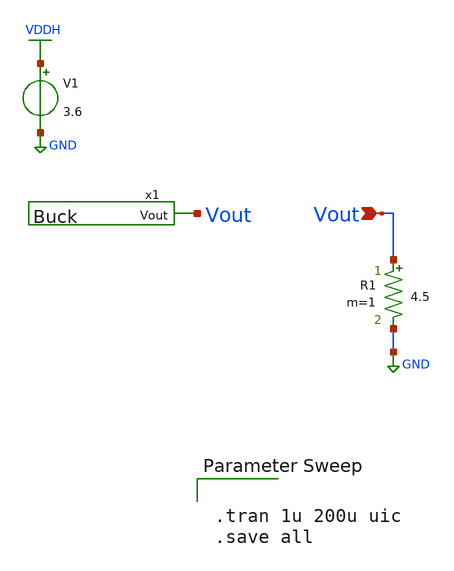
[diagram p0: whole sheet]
** sch_path: Ene_Thompson/test_Buck.sch
**.subckt test_Buck Vout
*.ipin Vout
x1 Vout Buck
V1 VDDH GND 3.6
R1 Vout GND 4.5 m=1
**** begin user architecture code

.lib $::SKYWATER_MODELS/sky130.lib.spice tt



.tran 1u 200u uic
.save all


**** end user architecture code
**.ends

* expanding   symbol:  Buck.sym # of pins=1
** sym_path: Ene_Thompson/Buck.sym
** sch_path: Ene_Thompson/Buck.sch
.subckt Buck Vout
*.opin Vout
XM1 vl net6 net1 VDDH sky130_fd_pr__pfet_g5v0d10v5 L=0.5 W=20 nf=1 ad='int((nf+1)/2) * W/nf * 0.29' as='int((nf+2)/2) * W/nf * 0.29'
+ pd='2*int((nf+1)/2) * (W/nf + 0.29)' ps='2*int((nf+2)/2) * (W/nf + 0.29)' nrd='0.29 / W' nrs='0.29 / W'
+ sa=0 sb=0 sd=0 mult=1025 m=1025
Xx3 vl net5 net4 GND sky130_fd_pr__nfet_g5v0d10v5 L=0.5 W=20 nf=1 ad='int((nf+1)/2) * W/nf * 0.29' as='int((nf+2)/2) * W/nf * 0.29'
+ pd='2*int((nf+1)/2) * (W/nf + 0.29)' ps='2*int((nf+2)/2) * (W/nf + 0.29)' nrd='0.29 / W' nrs='0.29 / W'
+ sa=0 sb=0 sd=0 mult=975 m=975
L1 net3 Vout 4.7u m=1
C1 Vout net2 1u m=1
V1 pswitch GND PULSE(0 3.6 0 0.01u 0.01u 0.435u 1u)
R1 vl net3 1.5m m=1
R2 GND net2 10m m=1
V2 nswitch GND PULSE(0 3.6 75n 0.01u 0.01u 0.285u 1u)
Vm1 VDDH net1 0
.save i(vm1)
Vm2 net4 GND 0
.save i(vm2)
x1 pswitch net6 drive_train
x2 nswitch net5 drive_train
.ends


* expanding   symbol:  drive_train.sym # of pins=2
** sym_path: Ene_Thompson/drive_train.sym
** sch_path: Ene_Thompson/drive_train.sch
.subckt drive_train A Y
*.opin Y
*.ipin A
XM1 net1 A GND GND sky130_fd_pr__nfet_g5v0d10v5 L=0.5 W=1 nf=1 ad='int((nf+1)/2) * W/nf * 0.29' as='int((nf+2)/2) * W/nf * 0.29'
+ pd='2*int((nf+1)/2) * (W/nf + 0.29)' ps='2*int((nf+2)/2) * (W/nf + 0.29)' nrd='0.29 / W' nrs='0.29 / W'
+ sa=0 sb=0 sd=0 mult=7 m=7
XM2 net1 A VDDH VDDH sky130_fd_pr__pfet_g5v0d10v5 L=0.5 W=1 nf=1 ad='int((nf+1)/2) * W/nf * 0.29' as='int((nf+2)/2) * W/nf * 0.29'
+ pd='2*int((nf+1)/2) * (W/nf + 0.29)' ps='2*int((nf+2)/2) * (W/nf + 0.29)' nrd='0.29 / W' nrs='0.29 / W'
+ sa=0 sb=0 sd=0 mult=7 m=7
XM3 net2 net1 GND GND sky130_fd_pr__nfet_g5v0d10v5 L=0.5 W=1 nf=1 ad='int((nf+1)/2) * W/nf * 0.29' as='int((nf+2)/2) * W/nf * 0.29'
+ pd='2*int((nf+1)/2) * (W/nf + 0.29)' ps='2*int((nf+2)/2) * (W/nf + 0.29)' nrd='0.29 / W' nrs='0.29 / W'
+ sa=0 sb=0 sd=0 mult=50 m=50
XM4 net2 net1 VDDH VDDH sky130_fd_pr__pfet_g5v0d10v5 L=0.5 W=1 nf=1 ad='int((nf+1)/2) * W/nf * 0.29'
+ as='int((nf+2)/2) * W/nf * 0.29' pd='2*int((nf+1)/2) * (W/nf + 0.29)' ps='2*int((nf+2)/2) * (W/nf + 0.29)'
+ nrd='0.29 / W' nrs='0.29 / W' sa=0 sb=0 sd=0 mult=50 m=50
XM5 net3 net2 GND GND sky130_fd_pr__nfet_g5v0d10v5 L=0.5 W=10 nf=1 ad='int((nf+1)/2) * W/nf * 0.29' as='int((nf+2)/2) * W/nf * 0.29'
+ pd='2*int((nf+1)/2) * (W/nf + 0.29)' ps='2*int((nf+2)/2) * (W/nf + 0.29)' nrd='0.29 / W' nrs='0.29 / W'
+ sa=0 sb=0 sd=0 mult=35 m=35
XM6 net3 net2 VDDH VDDH sky130_fd_pr__pfet_g5v0d10v5 L=0.5 W=10 nf=1 ad='int((nf+1)/2) * W/nf * 0.29'
+ as='int((nf+2)/2) * W/nf * 0.29' pd='2*int((nf+1)/2) * (W/nf + 0.29)' ps='2*int((nf+2)/2) * (W/nf + 0.29)'
+ nrd='0.29 / W' nrs='0.29 / W' sa=0 sb=0 sd=0 mult=35 m=35
XM7 Y net3 GND GND sky130_fd_pr__nfet_g5v0d10v5 L=0.5 W=20 nf=1 ad='int((nf+1)/2) * W/nf * 0.29' as='int((nf+2)/2) * W/nf * 0.29'
+ pd='2*int((nf+1)/2) * (W/nf + 0.29)' ps='2*int((nf+2)/2) * (W/nf + 0.29)' nrd='0.29 / W' nrs='0.29 / W'
+ sa=0 sb=0 sd=0 mult=125 m=125
XM8 Y net3 VDDH VDDH sky130_fd_pr__pfet_g5v0d10v5 L=0.5 W=20 nf=1 ad='int((nf+1)/2) * W/nf * 0.29' as='int((nf+2)/2) * W/nf * 0.29'
+ pd='2*int((nf+1)/2) * (W/nf + 0.29)' ps='2*int((nf+2)/2) * (W/nf + 0.29)' nrd='0.29 / W' nrs='0.29 / W'
+ sa=0 sb=0 sd=0 mult=125 m=125
.ends

.GLOBAL VDDH
.GLOBAL GND
.end
